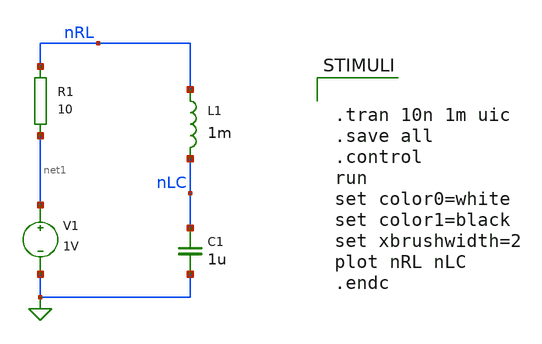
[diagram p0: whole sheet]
** sch_path: xschem_library/examples/new_spice_demo.sch
**.subckt new_spice_demo
R1 nRL net1 10
C1 nLC 0 1u
L1 nRL nLC 1m
V1 net1 0 1V
**** begin user architecture code


.tran 10n 1m uic
.save all
.control
run
set color0=white
set color1=black
set xbrushwidth=2
plot nRL nLC
.endc


**** end user architecture code
**.ends
.end
